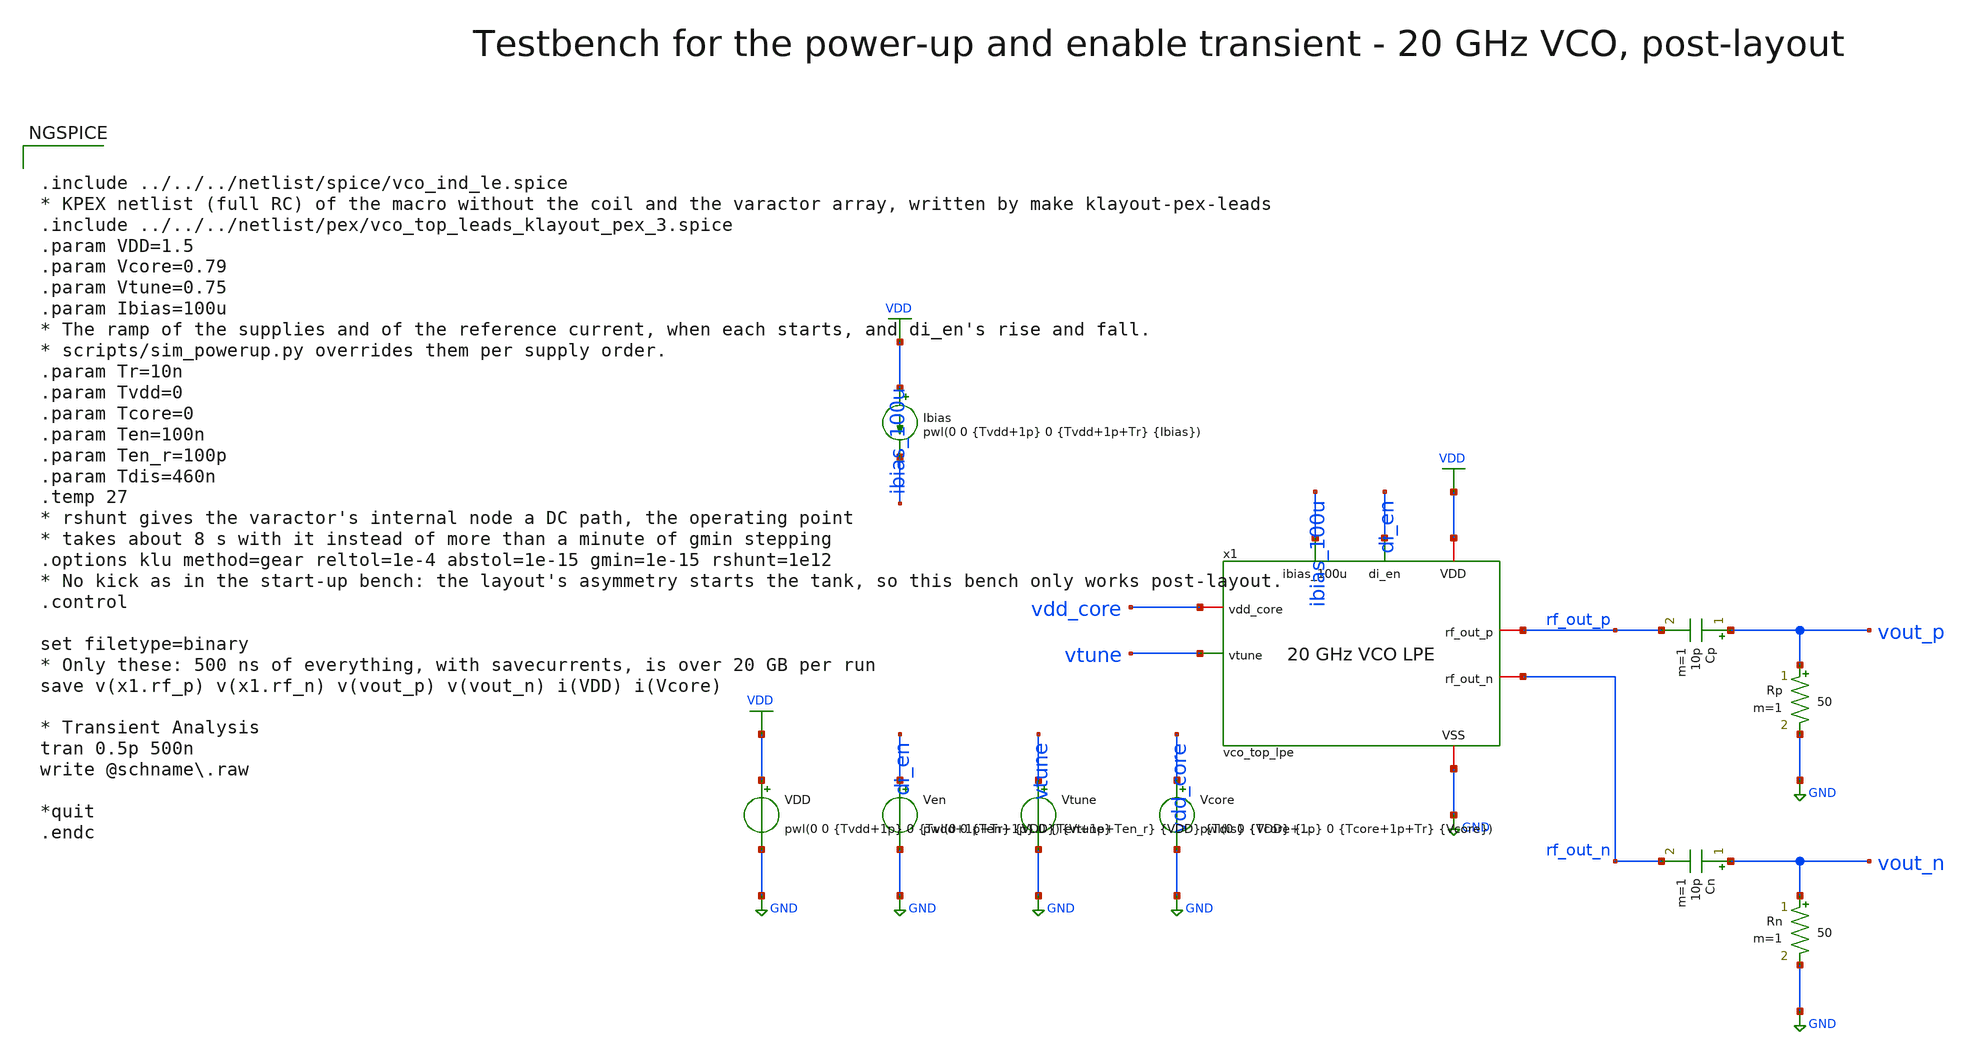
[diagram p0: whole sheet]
** sch_path: macros/vco/testbenches/xschem/vco_top_tb_powerup_lpe.sch
**.subckt vco_top_tb_powerup_lpe
x1 ibias_100u di_en VDD GND vdd_core vtune rf_out_p rf_out_n vco_top_lpe
Vcore vdd_core GND pwl(0 0 {Tcore+1p} 0 {Tcore+1p+Tr} {Vcore})
Cp vout_p rf_out_p 10p m=1
Rp vout_p GND 50 m=1
Cn vout_n rf_out_n 10p m=1
Rn vout_n GND 50 m=1
VDD VDD GND pwl(0 0 {Tvdd+1p} 0 {Tvdd+1p+Tr} {VDD})
Ven di_en GND pwl(0 0 {Ten+1p} 0 {Ten+1p+Ten_r} {VDD} {Tdis} {VDD} {Tdis+100p} 0)
Vtune vtune GND {Vtune}
Ibias VDD ibias_100u pwl(0 0 {Tvdd+1p} 0 {Tvdd+1p+Tr} {Ibias})
**** begin user architecture code


.include ../../../netlist/spice/vco_ind_le.spice
* KPEX netlist (full RC) of the macro without the coil and the varactor array, written by make
*+ klayout-pex-leads
.include ../../../netlist/pex/vco_top_leads_klayout_pex_3.spice
.param VDD=1.5
.param Vcore=0.79
.param Vtune=0.75
.param Ibias=100u
* The ramp of the supplies and of the reference current, when each starts, and di_en's rise and fall.
* scripts/sim_powerup.py overrides them per supply order.
.param Tr=10n
.param Tvdd=0
.param Tcore=0
.param Ten=100n
.param Ten_r=100p
.param Tdis=460n
.temp 27
* rshunt gives the varactor's internal node a DC path, the operating point
* takes about 8 s with it instead of more than a minute of gmin stepping
.options klu method=gear reltol=1e-4 abstol=1e-15 gmin=1e-15 rshunt=1e12
* No kick as in the start-up bench: the layout's asymmetry starts the tank, so this bench only works post-layout.
.control

set filetype=binary
* Only these: 500 ns of everything, with savecurrents, is over 20 GB per run
save v(x1.rf_p) v(x1.rf_n) v(vout_p) v(vout_n) i(VDD) i(Vcore)

* Transient Analysis
tran 0.5p 500n
write @schname\.raw

*quit
.endc



.lib cornerMOSlv.lib mos_tt
.lib cornerMOShv.lib mos_tt
.lib cornerRES.lib res_typ
.lib cornerCAP.lib cap_typ

**** end user architecture code
**.ends
.GLOBAL VDD
.GLOBAL GND
.end
